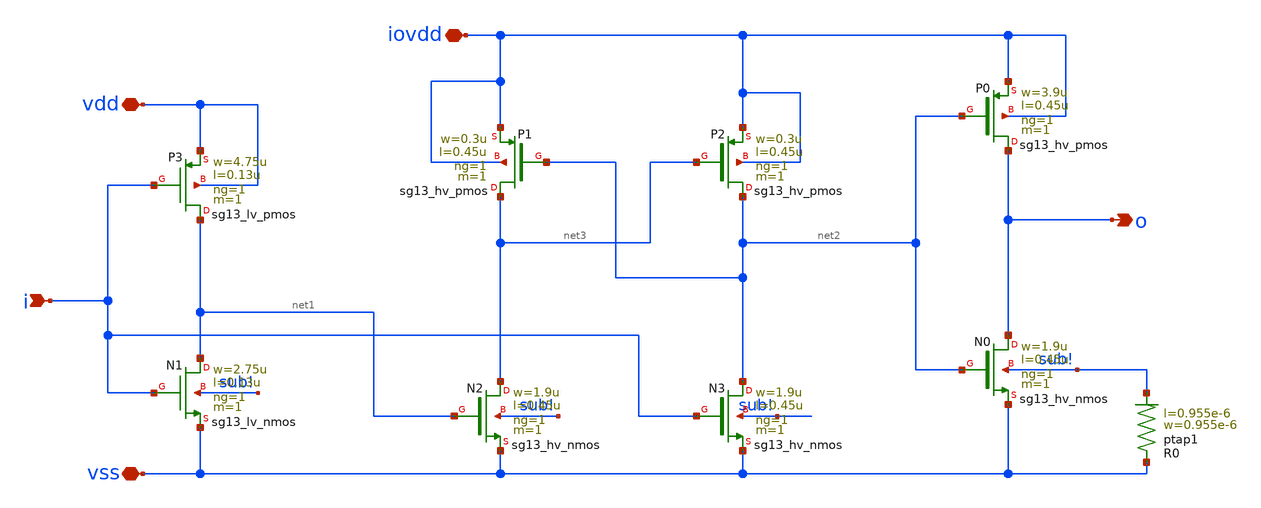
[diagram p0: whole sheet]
** sch_path: ihp-sg13g2/libs.ref/sg13g2_io/sch/xschem/sg13g2_LevelUp.sch
**.subckt sg13g2_LevelUp iovdd vss vdd i o
*.iopin iovdd
*.iopin vss
*.iopin vdd
*.ipin i
*.opin o
XN0 o net2 vss sub! sg13_hv_nmos w=1.9u l=0.45u ng=1 m=1 mm_ok=1
XN1 net1 i vss sub! sg13_lv_nmos w=2.75u l=0.13u ng=1 m=1 mm_ok=1
XN2 net3 net1 vss sub! sg13_hv_nmos w=1.9u l=0.45u ng=1 m=1 mm_ok=1
XN3 net2 i vss sub! sg13_hv_nmos w=1.9u l=0.45u ng=1 m=1 mm_ok=1
XP0 o net2 iovdd iovdd sg13_hv_pmos w=3.9u l=0.45u ng=1 m=1 mm_ok=1
XP1 net3 net2 iovdd iovdd sg13_hv_pmos w=0.3u l=0.45u ng=1 m=1 mm_ok=1
XP2 net2 net3 iovdd iovdd sg13_hv_pmos w=0.3u l=0.45u ng=1 m=1 mm_ok=1
XP3 net1 i vdd vdd sg13_lv_pmos w=4.75u l=0.13u ng=1 m=1 mm_ok=1
XR0 vss sub! ptap1 R=207.1 w=0.955e-6 l=0.955e-6
**.ends
.end
